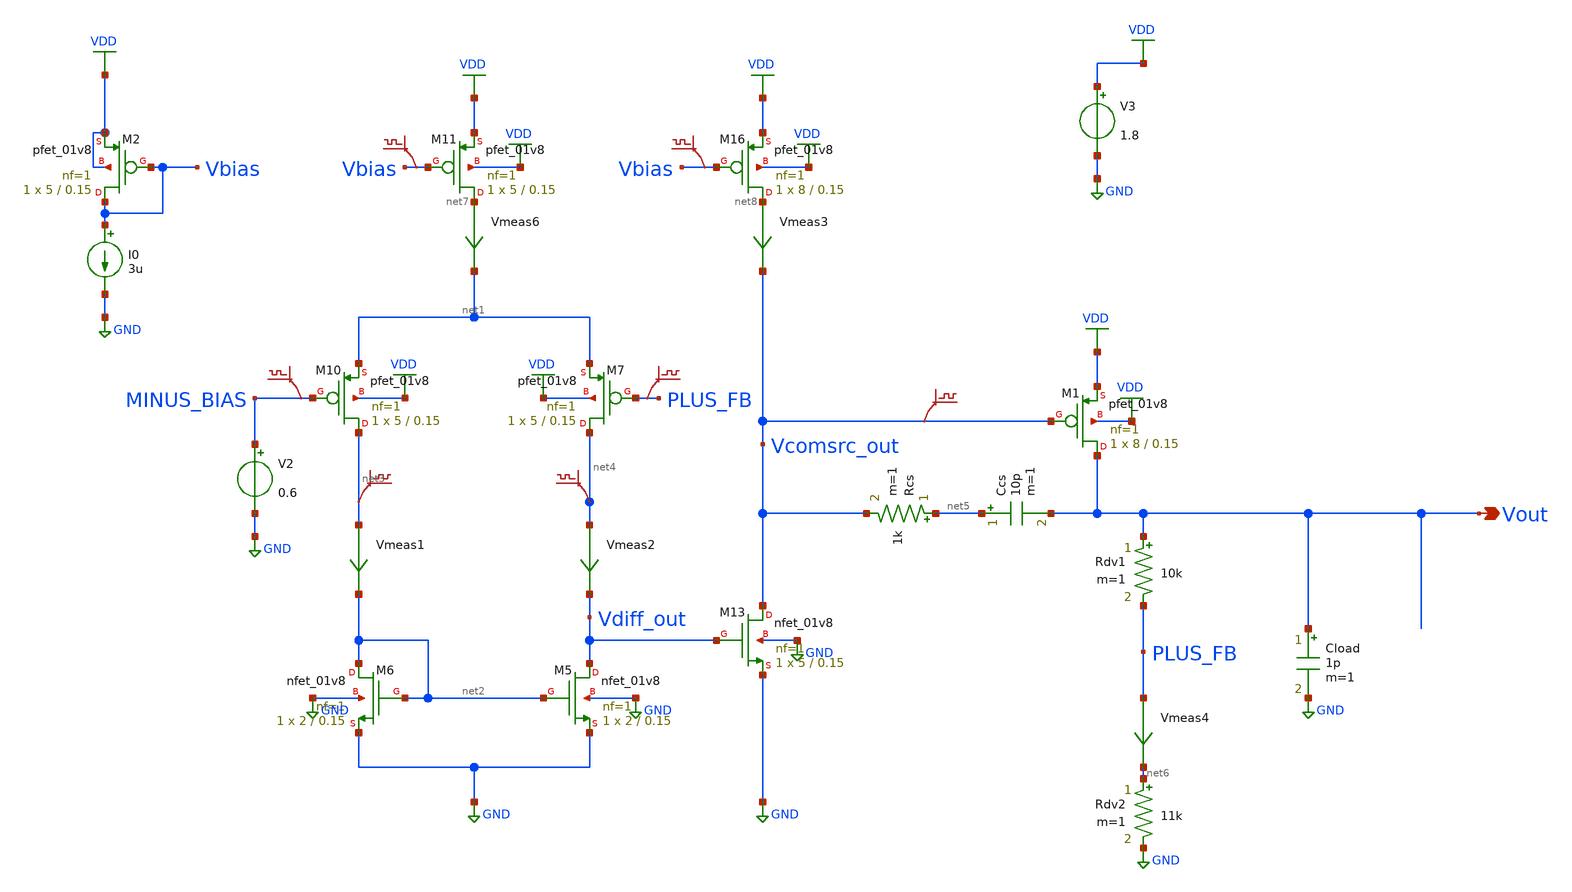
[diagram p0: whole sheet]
** sch_path: lib/xschem/LDO/LDO.sch
**.subckt LDO Vout
*.opin Vout
XM6 net2 net2 GND GND sky130_fd_pr__nfet_01v8 L=0.15 W=2 nf=1 ad='int((nf+1)/2) * W/nf * 0.29' as='int((nf+2)/2) * W/nf * 0.29'
+ pd='2*int((nf+1)/2) * (W/nf + 0.29)' ps='2*int((nf+2)/2) * (W/nf + 0.29)' nrd='0.29 / W' nrs='0.29 / W'
+ sa=0 sb=0 sd=0 mult=1 m=1
XM5 Vdiff_out net2 GND GND sky130_fd_pr__nfet_01v8 L=0.15 W=2 nf=1 ad='int((nf+1)/2) * W/nf * 0.29' as='int((nf+2)/2) * W/nf * 0.29'
+ pd='2*int((nf+1)/2) * (W/nf + 0.29)' ps='2*int((nf+2)/2) * (W/nf + 0.29)' nrd='0.29 / W' nrs='0.29 / W'
+ sa=0 sb=0 sd=0 mult=1 m=1
XM7 net4 PLUS_FB net1 VDD sky130_fd_pr__pfet_01v8 L=0.15 W=5 nf=1 ad='int((nf+1)/2) * W/nf * 0.29' as='int((nf+2)/2) * W/nf * 0.29'
+ pd='2*int((nf+1)/2) * (W/nf + 0.29)' ps='2*int((nf+2)/2) * (W/nf + 0.29)' nrd='0.29 / W' nrs='0.29 / W'
+ sa=0 sb=0 sd=0 mult=1 m=1
XM10 net3 MINUS_BIAS net1 VDD sky130_fd_pr__pfet_01v8 L=0.15 W=5 nf=1 ad='int((nf+1)/2) * W/nf * 0.29'
+ as='int((nf+2)/2) * W/nf * 0.29' pd='2*int((nf+1)/2) * (W/nf + 0.29)' ps='2*int((nf+2)/2) * (W/nf + 0.29)'
+ nrd='0.29 / W' nrs='0.29 / W' sa=0 sb=0 sd=0 mult=1 m=1
XM11 net7 Vbias VDD VDD sky130_fd_pr__pfet_01v8 L=0.15 W=5 nf=1 ad='int((nf+1)/2) * W/nf * 0.29' as='int((nf+2)/2) * W/nf * 0.29'
+ pd='2*int((nf+1)/2) * (W/nf + 0.29)' ps='2*int((nf+2)/2) * (W/nf + 0.29)' nrd='0.29 / W' nrs='0.29 / W'
+ sa=0 sb=0 sd=0 mult=1 m=1
XM13 Vcomsrc_out Vdiff_out GND GND sky130_fd_pr__nfet_01v8 L=0.15 W=5 nf=1 ad='int((nf+1)/2) * W/nf * 0.29'
+ as='int((nf+2)/2) * W/nf * 0.29' pd='2*int((nf+1)/2) * (W/nf + 0.29)' ps='2*int((nf+2)/2) * (W/nf + 0.29)'
+ nrd='0.29 / W' nrs='0.29 / W' sa=0 sb=0 sd=0 mult=1 m=1
XM16 net8 Vbias VDD VDD sky130_fd_pr__pfet_01v8 L=0.15 W=8 nf=1 ad='int((nf+1)/2) * W/nf * 0.29' as='int((nf+2)/2) * W/nf * 0.29'
+ pd='2*int((nf+1)/2) * (W/nf + 0.29)' ps='2*int((nf+2)/2) * (W/nf + 0.29)' nrd='0.29 / W' nrs='0.29 / W'
+ sa=0 sb=0 sd=0 mult=1 m=1
V2 MINUS_BIAS GND 0.6
V3 VDD GND 1.8
.save v(plus_fb)
.save v(minus_bias)
.save v(net4)
.save v(net3)
.save v(vcomsrc_out)
Vmeas1 net3 net2 0
.save i(vmeas1)
Vmeas2 net4 Vdiff_out 0
.save i(vmeas2)
Vmeas3 net8 Vcomsrc_out 0
.save i(vmeas3)
.save v(vbias)
.save v(vbias)
Rdv1 Vout PLUS_FB 10k m=1
Rdv2 net6 GND 11k m=1
Vmeas4 PLUS_FB net6 0
.save i(vmeas4)
Vmeas6 net7 net1 0
.save i(vmeas6)
XM2 Vbias Vbias VDD VDD sky130_fd_pr__pfet_01v8 L=0.15 W=5 nf=1 ad='int((nf+1)/2) * W/nf * 0.29' as='int((nf+2)/2) * W/nf * 0.29'
+ pd='2*int((nf+1)/2) * (W/nf + 0.29)' ps='2*int((nf+2)/2) * (W/nf + 0.29)' nrd='0.29 / W' nrs='0.29 / W'
+ sa=0 sb=0 sd=0 mult=1 m=1
I0 Vbias GND 3u
Rcs net5 Vcomsrc_out 1k m=1
Ccs net5 Vout 10p m=1
Cload Vout GND 1p m=1
XM1 Vout Vcomsrc_out VDD VDD sky130_fd_pr__pfet_01v8 L=0.15 W=8 nf=1 ad='int((nf+1)/2) * W/nf * 0.29'
+ as='int((nf+2)/2) * W/nf * 0.29' pd='2*int((nf+1)/2) * (W/nf + 0.29)' ps='2*int((nf+2)/2) * (W/nf + 0.29)'
+ nrd='0.29 / W' nrs='0.29 / W' sa=0 sb=0 sd=0 mult=1 m=1
**** begin user architecture code

.lib $::SKYWATER_MODELS/sky130.lib.spice tt


**** end user architecture code
**.ends
.GLOBAL VDD
.GLOBAL GND
**** begin user architecture code


.save all
.op
.dc V3 1.5 2 0.1


**** end user architecture code
.end
